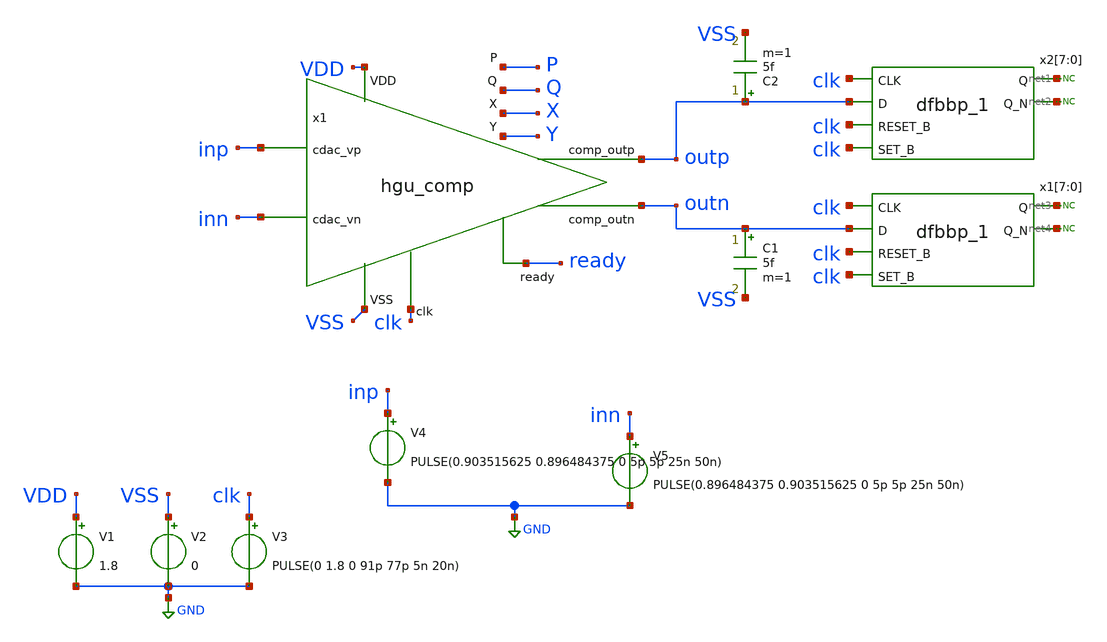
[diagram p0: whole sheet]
** sch_path: hgu/tb/tb_hgu_comp.sch
**.subckt tb_hgu_comp
x1 ready inn outp outn inp clk VDD VSS Q X Y P hgu_comp
V1 VDD GND 1.8
V2 VSS GND 0
V3 clk GND PULSE(0 1.8 0 91p 77p 5n 20n)
V4 inp GND PULSE(0.903515625 0.896484375 0 5p 5p 25n 50n)
V5 inn GND PULSE(0.896484375 0.903515625 0 5p 5p 25n 50n)
x2[7] clk outp clk clk VGND VNB VPB VPWR net1 net2 sky130_fd_sc_hd__dfbbp_1
x2[6] clk outp clk clk VGND VNB VPB VPWR net1 net2 sky130_fd_sc_hd__dfbbp_1
x2[5] clk outp clk clk VGND VNB VPB VPWR net1 net2 sky130_fd_sc_hd__dfbbp_1
x2[4] clk outp clk clk VGND VNB VPB VPWR net1 net2 sky130_fd_sc_hd__dfbbp_1
x2[3] clk outp clk clk VGND VNB VPB VPWR net1 net2 sky130_fd_sc_hd__dfbbp_1
x2[2] clk outp clk clk VGND VNB VPB VPWR net1 net2 sky130_fd_sc_hd__dfbbp_1
x2[1] clk outp clk clk VGND VNB VPB VPWR net1 net2 sky130_fd_sc_hd__dfbbp_1
x2[0] clk outp clk clk VGND VNB VPB VPWR net1 net2 sky130_fd_sc_hd__dfbbp_1
x1[7] clk outn clk clk VGND VNB VPB VPWR net3 net4 sky130_fd_sc_hd__dfbbp_1
x1[6] clk outn clk clk VGND VNB VPB VPWR net3 net4 sky130_fd_sc_hd__dfbbp_1
x1[5] clk outn clk clk VGND VNB VPB VPWR net3 net4 sky130_fd_sc_hd__dfbbp_1
x1[4] clk outn clk clk VGND VNB VPB VPWR net3 net4 sky130_fd_sc_hd__dfbbp_1
x1[3] clk outn clk clk VGND VNB VPB VPWR net3 net4 sky130_fd_sc_hd__dfbbp_1
x1[2] clk outn clk clk VGND VNB VPB VPWR net3 net4 sky130_fd_sc_hd__dfbbp_1
x1[1] clk outn clk clk VGND VNB VPB VPWR net3 net4 sky130_fd_sc_hd__dfbbp_1
x1[0] clk outn clk clk VGND VNB VPB VPWR net3 net4 sky130_fd_sc_hd__dfbbp_1
C1 outn VSS 5f m=1
C2 outp VSS 5f m=1
* noconn #net1
* noconn #net2
* noconn #net3
* noconn #net4
**** begin user architecture code


.include /foss/designs/hgu_goss/hgu/spice/hgu_comp_flat_RC.spice
.lib /foss/pdks/sky130A/libs.tech/ngspice/sky130.lib.spice tt
.include /foss/pdks/sky130A/libs.ref/sky130_fd_sc_hd/spice/sky130_fd_sc_hd.spice
.tran 1ns 100ns
.temp 25
.control
    run
     let svdd = 1.8
     let max = svdd*0.8
     let min = svdd*0.2
     let mid = svdd*0.5

   meas tran rising_s_d find time when V(clk)=mid RISE=1 TD=30n
   meas tran rising_e_d find time when V(outp)=mid RISE=1 TD=1000p
   let rising_delay = rising_e_d-rising_s_d

   meas tran falling_s_d find time when V(clk)=mid RISE=1 TD=50n
   meas tran falling_e_d find time when V(outp)=mid FALL=1 TD=50n
   let falling_delay = falling_e_d-falling_s_d

   meas tran rising_s find time when V(outp)=min RISE=1 TD=30n
      meas tran rising_e find time when V(outp)=max RISE=1 TD=30n
      let rising_time = rising_e-rising_s

      meas tran falling_s find time when V(outp)=max FALL=1 TD=50n
     meas tran falling_e find time when V(outp)=min FALL=1 TD=50n
      let falling_time = falling_e-falling_s

    print rising_time falling_time rising_delay falling_delay
    plot V(clk) V(inn) V(inp) V(ready) V(outp)+2 V(outn)+2
    plot V(outp) V(outn)
.endc
.save all


**** end user architecture code
**.ends
.GLOBAL GND
.end
